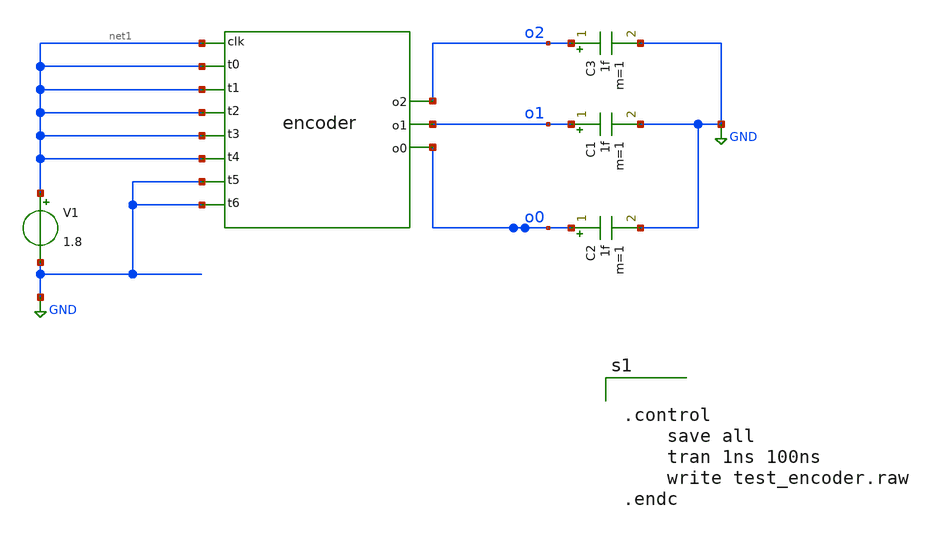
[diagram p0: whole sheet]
** sch_path: tt_um_emmersonv_tiq_adc/xschem/test_encoder.sch
**.subckt test_encoder
V1 net1 GND 1.8
C1 o1 GND 1f m=1
C2 o0 GND 1f m=1
C3 o2 GND 1f m=1
x1 [ net1 net1 net1 net1 net1 net1 GND GND ] [ o0 o1 o2 ] encoder
**** begin user architecture code


.control
	save all
	tran 1ns 100ns
	write test_encoder.raw
.endc


**** end user architecture code
**.ends
.GLOBAL GND
.end
